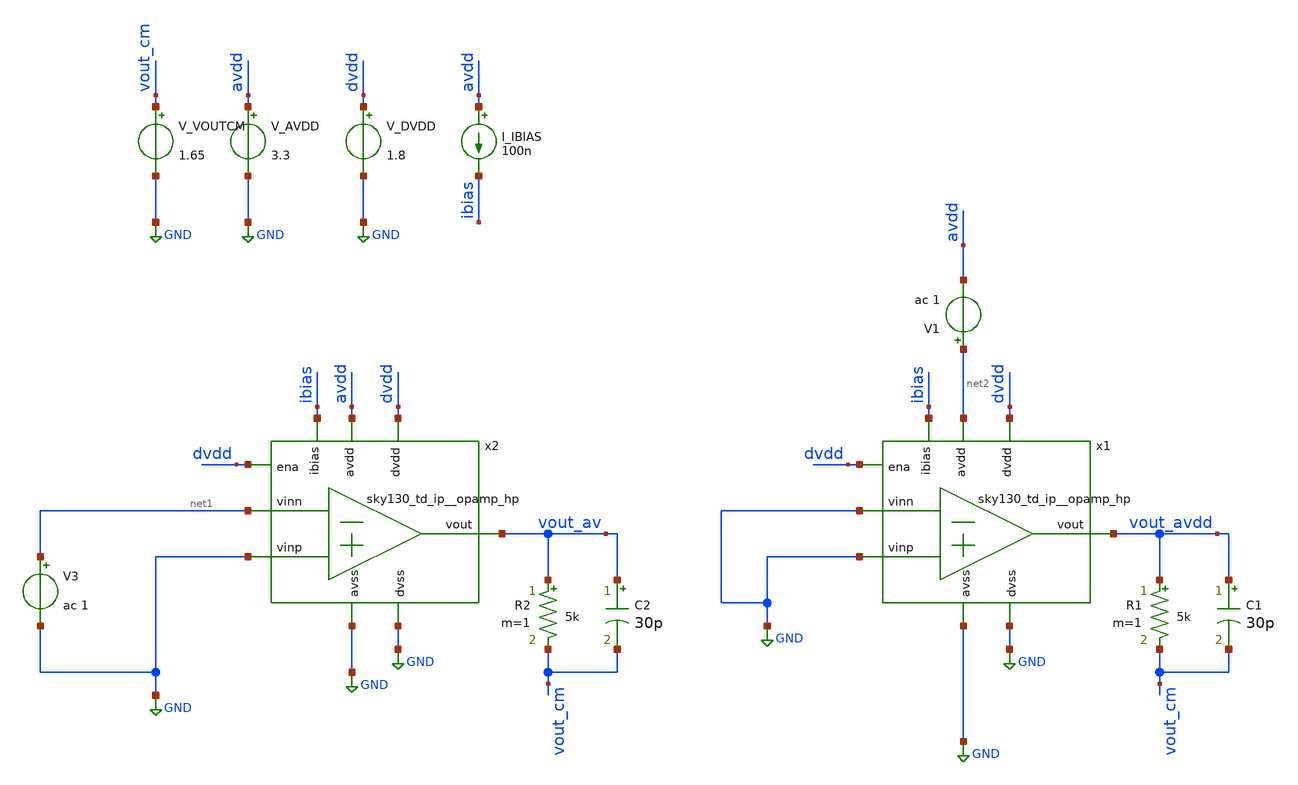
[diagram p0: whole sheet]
** sch_path: xschem/psrrp.sch
**.subckt psrrp
x1 net2 vout_avdd ibias GND GND GND dvdd GND dvdd sky130_td_ip__opamp_hp
V_AVDD avdd GND 3.3
.save i(v_avdd)
V_DVDD dvdd GND 1.8
.save i(v_dvdd)
I_IBIAS avdd ibias 100n
R1 vout_avdd vout_cm 5k m=1
C1 vout_avdd vout_cm 30p m=1
V_VOUTCM vout_cm GND 1.65
.save i(v_voutcm)
V1 net2 avdd ac 1
x2 avdd vout_av ibias net1 GND GND dvdd GND dvdd sky130_td_ip__opamp_hp
R2 vout_av vout_cm 5k m=1
C2 vout_av vout_cm 30p m=1
V3 net1 GND ac 1
**** begin user architecture code


.save all

.control
save all

* Run AC sweep from 1Hz to 1GHz
AC DEC 100 1 1000000000
run

* Get DC gain in DBs.
let av_db = db(vout_av)
let avdd_db = db(vout_avdd)
let psrrp_db = av_db - avdd_db

meas AC psrrp_dc FIND psrrp_db AT=1
meas AC psrrp_100k FIND psrrp_db AT=100K

echo
echo ===================================
echo PSRR+ characterization results:
echo - PSRR @ 1 Hz: $&psrrp_dc
echo - PSRR @ 100 kHz: $&psrrp_100k
echo ===================================


plot psrrp_db

.endc




.lib /usr/local/share/pdk/sky130A/libs.tech/combined/sky130.lib.spice tt


**** end user architecture code
**.ends
.GLOBAL GND
.end
